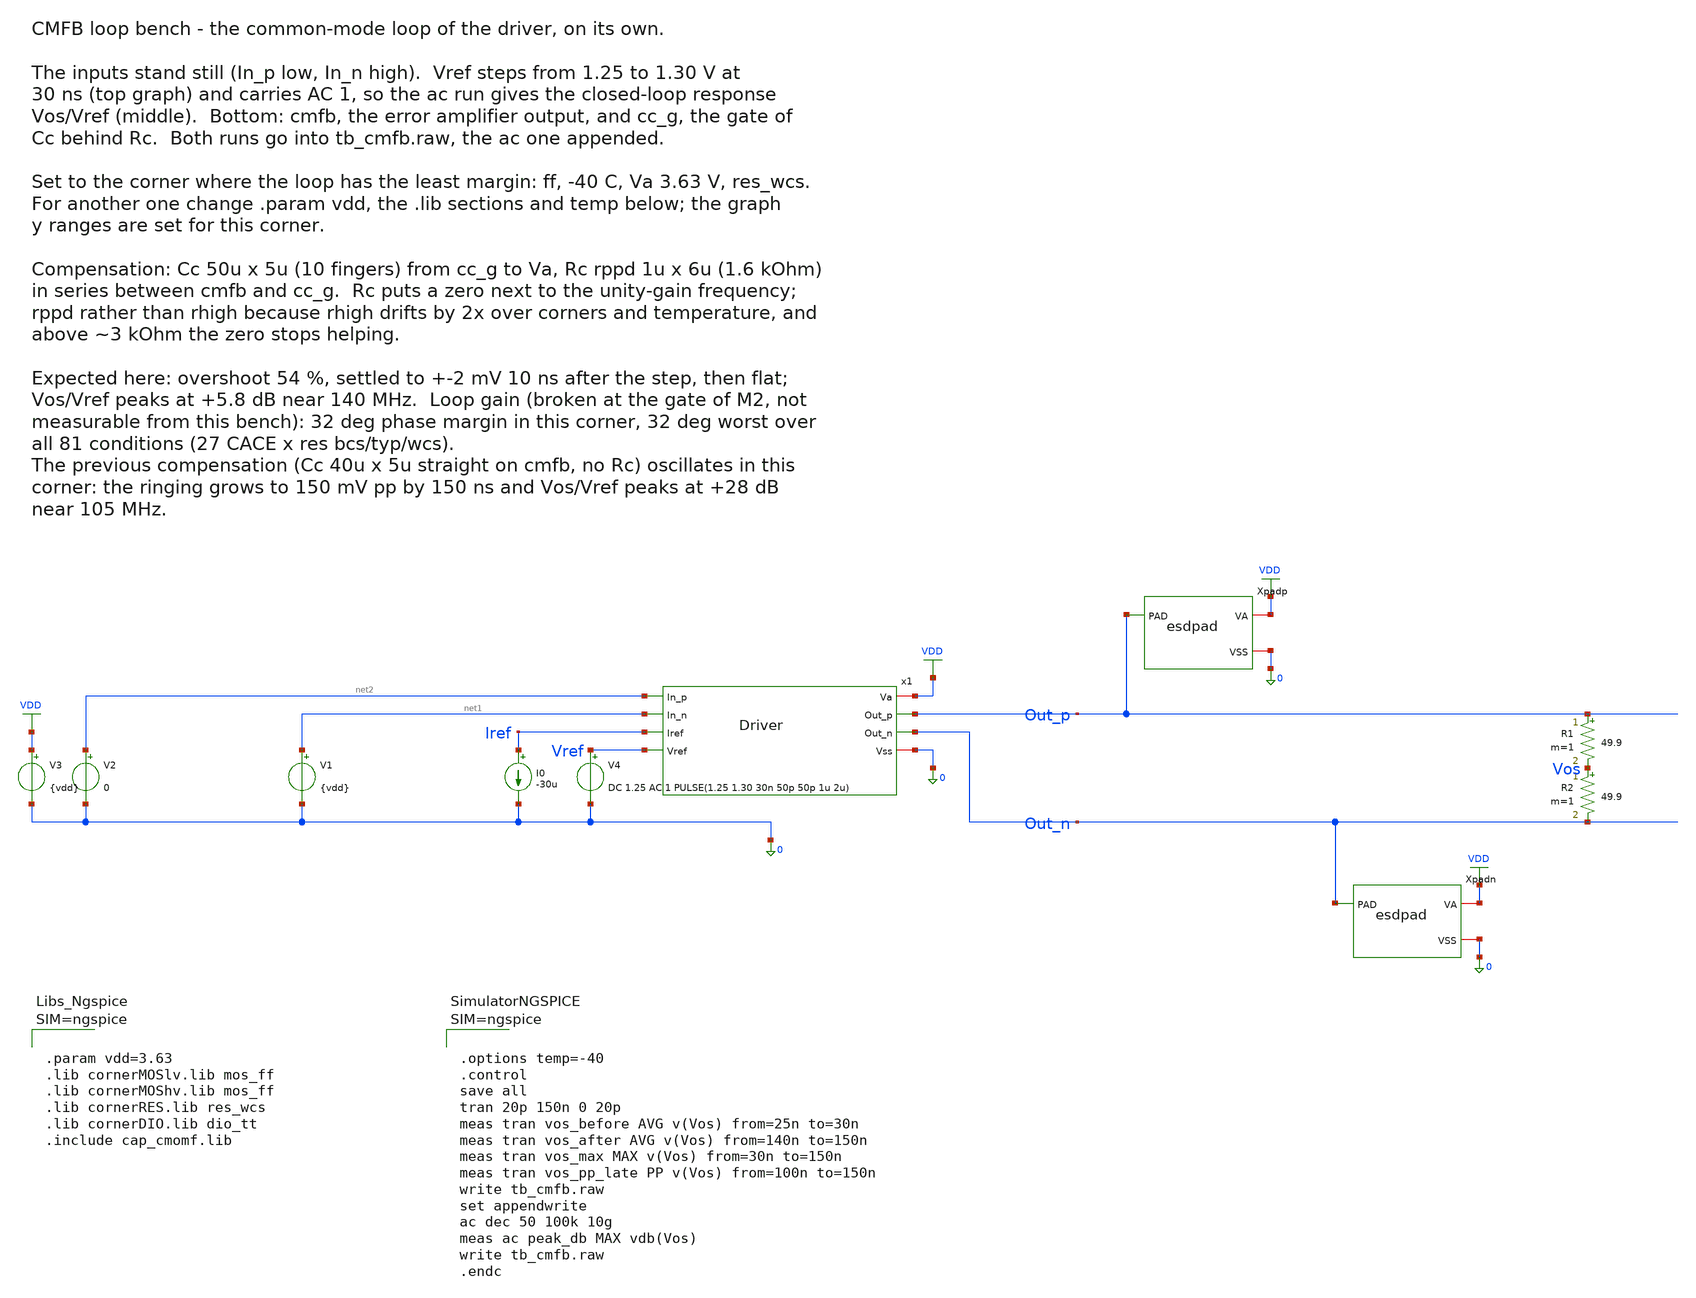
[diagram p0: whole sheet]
** sch_path: macros/lvds_tx/testbenches/xschem/tb_cmfb.sch
**.subckt tb_cmfb
x1 VDD Out_p net2 net1 Iref Vref Out_n 0 Driver
Xpadp Out_p VDD 0 esdpad
Xpadn Out_n VDD 0 esdpad
R1 Out_p Vos 49.9 m=1
R2 Vos Out_n 49.9 m=1
I0 Iref 0 -30u
V1 net1 0 {vdd}
V2 net2 0 0
V3 VDD 0 {vdd}
V4 Vref 0 DC 1.25 AC 1 PULSE(1.25 1.30 30n 50p 50p 1u 2u)
**** begin user architecture code



.param vdd=3.63
.lib cornerMOSlv.lib mos_ff
.lib cornerMOShv.lib mos_ff
.lib cornerRES.lib res_wcs
.lib cornerDIO.lib dio_tt
.include cap_cmomf.lib






.options temp=-40
.control
save all
tran 20p 150n 0 20p
meas tran vos_before AVG v(Vos) from=25n to=30n
meas tran vos_after AVG v(Vos) from=140n to=150n
meas tran vos_max MAX v(Vos) from=30n to=150n
meas tran vos_pp_late PP v(Vos) from=100n to=150n
write tb_cmfb.raw
set appendwrite
ac dec 50 100k 10g
meas ac peak_db MAX vdb(Vos)
write tb_cmfb.raw
.endc



**** end user architecture code
**.ends

* expanding   symbol:  Driver.sym # of pins=8
** sym_path: macros/lvds_tx/schematic/xschem/Driver.sym
** sch_path: macros/lvds_tx/schematic/xschem/Driver.sch
.subckt Driver Va Out_p In_p In_n Iref Vref Out_n Vss
*.iopin Va
*.iopin Vss
*.opin Out_p
*.opin Out_n
*.ipin In_p
*.ipin In_n
*.ipin Iref
*.ipin Vref
XCtn1 Va tail_n Va Va sg13_hv_pmos w=11.8u l=5.25u ng=2 m=1 mm_ok=1
XCtn2 Va tail_n Va Va sg13_hv_pmos w=5.7u l=5.8u ng=2 m=1 mm_ok=1
XM2 tail_p cmfb Va Va sg13_hv_pmos w=97.2u l=0.5u ng=20 m=1 mm_ok=1
XM5 Out_p In_p tail_p Va sg13_hv_pmos w=80u l=0.4u ng=16 m=1 mm_ok=1
XM4 Out_n In_n tail_p Va sg13_hv_pmos w=80u l=0.4u ng=16 m=1 mm_ok=1
XM1 Out_p In_p tail_n Vss sg13_hv_nmos w=30u l=0.45u ng=15 m=1 mm_ok=1
XM3 Out_n In_n tail_n Vss sg13_hv_nmos w=30u l=0.45u ng=15 m=1 mm_ok=1
XM6 tail_n Iref Vss Vss sg13_hv_nmos w=49.6u l=0.5u ng=31 m=2 mm_ok=1
XM9 Iref Iref Vss Vss sg13_hv_nmos w=0.8u l=0.5u ng=1 m=1 mm_ok=1
XM13 pd pd Va Va sg13_hv_pmos w=5u l=1u ng=1 m=1 mm_ok=1
XM14 cmfb pd Va Va sg13_hv_pmos w=5u l=1u ng=1 m=1 mm_ok=1
XM11 pd cm otail Vss sg13_hv_nmos w=40u l=1u ng=16 m=1 mm_ok=1
XM12 cmfb Vref otail Vss sg13_hv_nmos w=40u l=1u ng=16 m=1 mm_ok=1
XM10 otail Iref Vss Vss sg13_hv_nmos w=0.8u l=0.5u ng=1 m=1 mm_ok=1
XCc Va cc_g Va Va sg13_hv_pmos w=50u l=5u ng=10 m=1 mm_ok=1
XRc cmfb cc_g Vss rppd w=1u l=6u m=1 b=0 mm_ok=1
XRp Out_p cm Vss rhigh w=1u l=7.35u m=1 b=0 mm_ok=1
XRn Out_n cm Vss rhigh w=1u l=7.35u m=1 b=0 mm_ok=1
XCxp Out_p In_n cap_cmomf w=5.913u l=5.913u mmin=1 mmax=4 subblock=0 rfmodel=0 subscale=1 m=1
+ mm_ok=1
XCxn Out_n In_p cap_cmomf w=5.913u l=5.913u mmin=1 mmax=4 subblock=0 rfmodel=0 subscale=1 m=1
+ mm_ok=1
XCop Vss Out_p Vss Vss sg13_hv_nmos w=10u l=5u ng=1 m=2 mm_ok=1
XCon Vss Out_n Vss Vss sg13_hv_nmos w=10u l=5u ng=1 m=2 mm_ok=1
.ends


* expanding   symbol:  esdpad.sym # of pins=3
** sym_path: macros/lvds_tx/schematic/xschem/esdpad.sym
** sch_path: macros/lvds_tx/schematic/xschem/esdpad.sch
.subckt esdpad PAD VA VSS
*.iopin PAD
*.iopin VA
*.iopin VSS
XDdvdd VA PAD VSS diodevdd_4kv m=1
XDdvss VA PAD VSS diodevss_4kv m=1
Cpad PAD VSS 90f m=1
.ends

.GLOBAL VDD
.end
